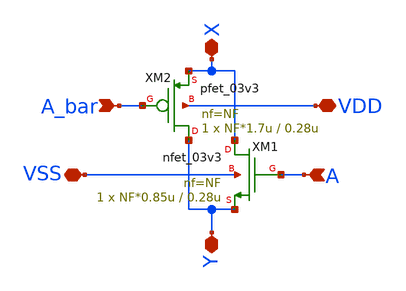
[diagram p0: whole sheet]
** sch_path: xschem_lib/DFFRAM_full_custom/tr_gate.sch
**.subckt tr_gate VSS A_bar VDD A X Y
*.iopin VSS
*.ipin A_bar
*.iopin VDD
*.ipin A
*.iopin X
*.iopin Y
XM1 X A Y VSS nfet_03v3 L=0.28u W=NF*0.85u nf=NF ad='int((nf+1)/2) * W/nf * 0.18u' as='int((nf+2)/2) * W/nf * 0.18u'
+ pd='2*int((nf+1)/2) * (W/nf + 0.18u)' ps='2*int((nf+2)/2) * (W/nf + 0.18u)' nrd='0.18u / W' nrs='0.18u / W'
+ sa=0 sb=0 sd=0 m=1
XM2 Y A_bar X VDD pfet_03v3 L=0.28u W=NF*1.7u nf=NF ad='int((nf+1)/2) * W/nf * 0.18u' as='int((nf+2)/2) * W/nf * 0.18u'
+ pd='2*int((nf+1)/2) * (W/nf + 0.18u)' ps='2*int((nf+2)/2) * (W/nf + 0.18u)' nrd='0.18u / W' nrs='0.18u / W'
+ sa=0 sb=0 sd=0 m=1
**.ends
.end
